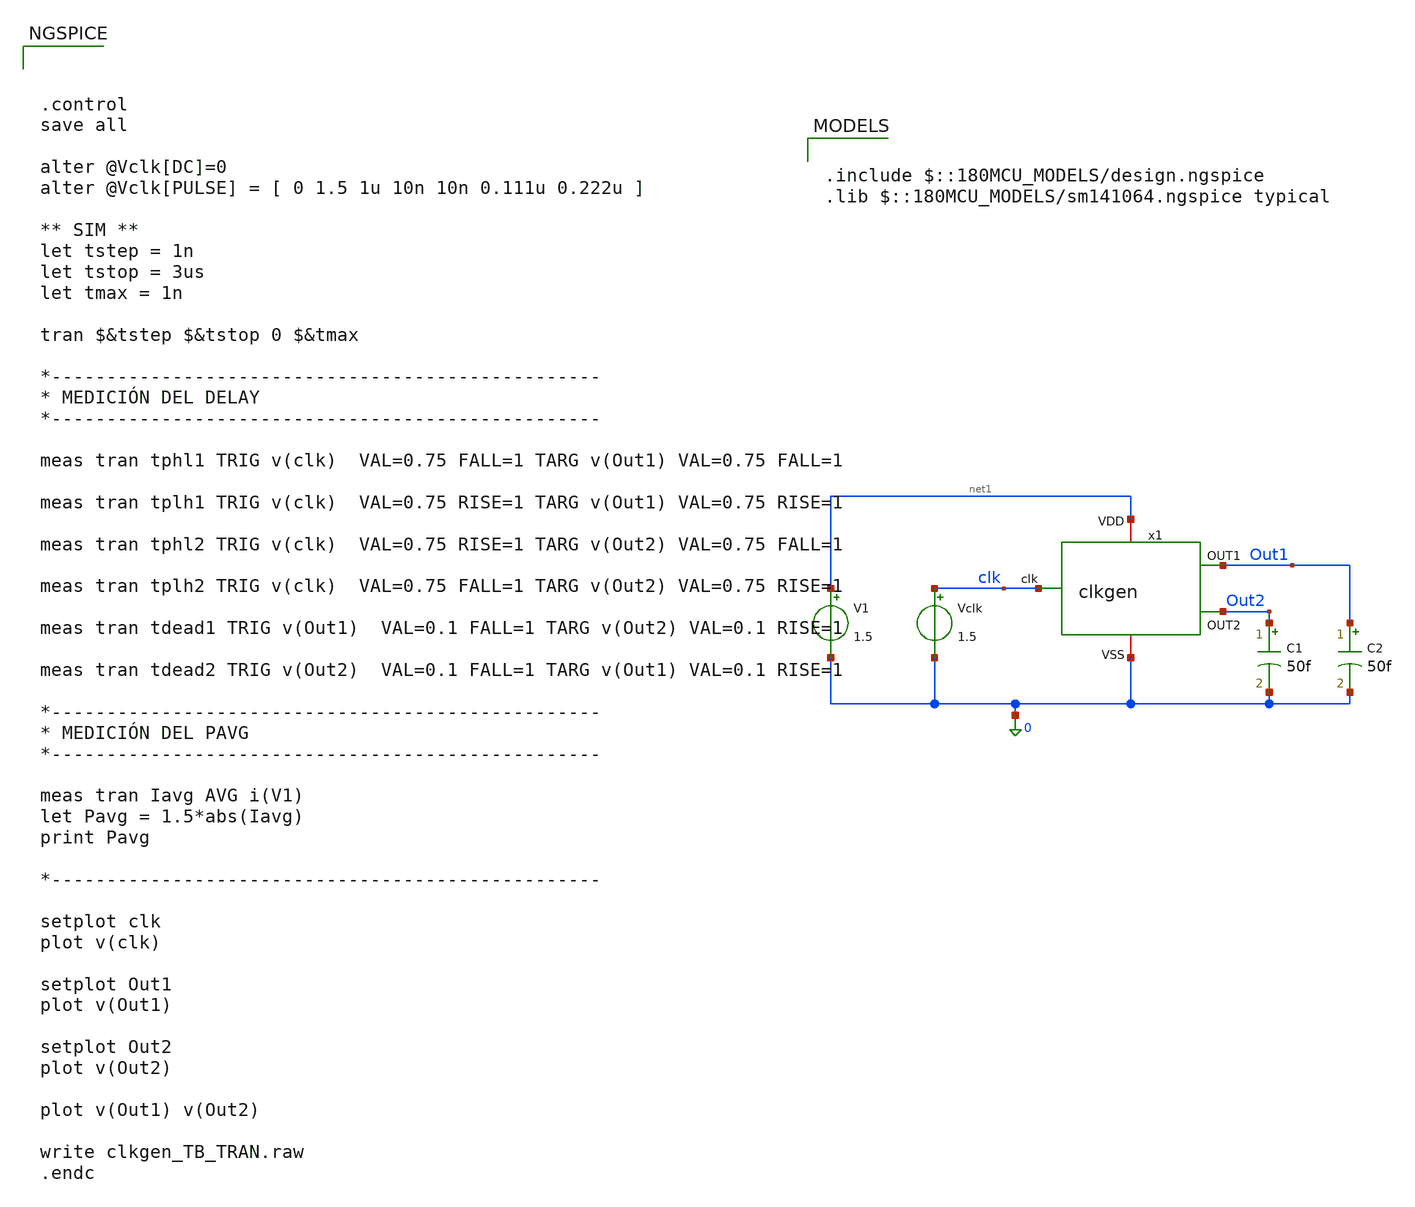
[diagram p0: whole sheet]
** sch_path: designs/DS_modulator/clkgen/xscheme/clkgen_TB_TRAN.sch
**.subckt clkgen_TB_TRAN
x1 net1 clk Out1 Out2 0 clkgen
V1 net1 0 1.5
Vclk clk 0 1.5
C1 Out2 0 50f m=1
C2 Out1 0 50f m=1
**** begin user architecture code

.include $::180MCU_MODELS/design.ngspice
.lib $::180MCU_MODELS/sm141064.ngspice typical




.control
save all

alter @Vclk[DC]=0
alter @Vclk[PULSE] = [ 0 1.5 1u 10n 10n 0.111u 0.222u ]

** SIM **
let tstep = 1n
let tstop = 3us
let tmax = 1n

tran $&tstep $&tstop 0 $&tmax

*--------------------------------------------------
* MEDICIÓN DEL DELAY
*--------------------------------------------------

meas tran tphl1 TRIG v(clk)  VAL=0.75 FALL=1 TARG v(Out1) VAL=0.75 FALL=1

meas tran tplh1 TRIG v(clk)  VAL=0.75 RISE=1 TARG v(Out1) VAL=0.75 RISE=1

meas tran tphl2 TRIG v(clk)  VAL=0.75 RISE=1 TARG v(Out2) VAL=0.75 FALL=1

meas tran tplh2 TRIG v(clk)  VAL=0.75 FALL=1 TARG v(Out2) VAL=0.75 RISE=1

meas tran tdead1 TRIG v(Out1)  VAL=0.1 FALL=1 TARG v(Out2) VAL=0.1 RISE=1

meas tran tdead2 TRIG v(Out2)  VAL=0.1 FALL=1 TARG v(Out1) VAL=0.1 RISE=1

*--------------------------------------------------
* MEDICIÓN DEL PAVG
*--------------------------------------------------

meas tran Iavg AVG i(V1)
let Pavg = 1.5*abs(Iavg)
print Pavg

*--------------------------------------------------

setplot clk
plot v(clk)

setplot Out1
plot v(Out1)

setplot Out2
plot v(Out2)

plot v(Out1) v(Out2)

write clkgen_TB_TRAN.raw
.endc


**** end user architecture code
**.ends

* expanding   symbol:
*+  chipaton/chipa2026_gf180mcu_DeltaSigma/designs/DS_modulator/clkgen/xscheme/clkgen.sym # of pins=5
** sym_path: chipaton/chipa2026_gf180mcu_DeltaSigma/designs/DS_modulator/clkgen/xscheme/clkgen.sym
** sch_path: chipaton/chipa2026_gf180mcu_DeltaSigma/designs/DS_modulator/clkgen/xscheme/clkgen.sch
.subckt clkgen VDD clk OUT1 OUT2 VSS
*.ipin clk
*.opin OUT1
*.opin OUT2
*.iopin VDD
*.iopin VSS
x1 VDD net3 net6 VSS gate_inv_L0d28
x2 VDD net4 net3 VSS gate_inv_L0d28
x3 VDD net1 net5 VSS gate_inv_L0d28
x4 VDD net2 net1 VSS gate_inv_L0d28
x5 VDD OUT2 net4 VSS gate_inv_L0d28
x6 VDD OUT1 net2 VSS gate_inv_L0d28
x7 VDD net7 clk VSS gate_inv_L0d28
x8 VDD net8 net9 net10 VDD clkgen_nand
x9 net11 net12 net13 net14 net15 clkgen_nand
.ends


* expanding   symbol:
*+  chipaton/chipa2026_gf180mcu_DeltaSigma/designs/DS_modulator/gate_inv_L0d28/xschem/gate_inv_L0d28.sym # of pins=4
** sym_path: chipaton/chipa2026_gf180mcu_DeltaSigma/designs/DS_modulator/gate_inv_L0d28/xschem/gate_inv_L0d28.sym
** sch_path: chipaton/chipa2026_gf180mcu_DeltaSigma/designs/DS_modulator/gate_inv_L0d28/xschem/gate_inv_L0d28.sch
.subckt gate_inv_L0d28 VDD B A VSS
*.opin B
*.ipin A
*.iopin VDD
*.iopin VSS
XMN B A VSS VSS nfet_03v3 L=0.28u W=1u nf=1 ad='int((nf+1)/2) * W/nf * 0.18u' as='int((nf+2)/2) * W/nf * 0.18u'
+ pd='2*int((nf+1)/2) * (W/nf + 0.18u)' ps='2*int((nf+2)/2) * (W/nf + 0.18u)' nrd='0.18u / W' nrs='0.18u / W'
+ sa=0 sb=0 sd=0 m=2
XMP B A VDD VDD pfet_03v3 L=0.28u W=3u nf=1 ad='int((nf+1)/2) * W/nf * 0.18u' as='int((nf+2)/2) * W/nf * 0.18u'
+ pd='2*int((nf+1)/2) * (W/nf + 0.18u)' ps='2*int((nf+2)/2) * (W/nf + 0.18u)' nrd='0.18u / W' nrs='0.18u / W'
+ sa=0 sb=0 sd=0 m=2
.ends


* expanding   symbol:
*+  chipaton/chipa2026_gf180mcu_DeltaSigma/designs/DS_modulator/clkgen/xscheme/clkgen_nand.sym # of pins=5
** sym_path: chipaton/chipa2026_gf180mcu_DeltaSigma/designs/DS_modulator/clkgen/xscheme/clkgen_nand.sym
** sch_path: chipaton/chipa2026_gf180mcu_DeltaSigma/designs/DS_modulator/clkgen/xscheme/clkgen_nand.sch
.subckt clkgen_nand VDD IN1 OUT IN2 VSS
*.ipin IN1
*.opin OUT
*.iopin VDD
*.ipin IN2
*.iopin VSS
XM1 net1 IN2 VSS VSS nfet_03v3 L=0.28u W=0.22u nf=1 ad='int((nf+1)/2) * W/nf * 0.18u' as='int((nf+2)/2) * W/nf * 0.18u'
+ pd='2*int((nf+1)/2) * (W/nf + 0.18u)' ps='2*int((nf+2)/2) * (W/nf + 0.18u)' nrd='0.18u / W' nrs='0.18u / W'
+ sa=0 sb=0 sd=0 m=1
XM2 OUT IN1 net1 VSS nfet_03v3 L=0.28u W=0.22u nf=1 ad='int((nf+1)/2) * W/nf * 0.18u' as='int((nf+2)/2) * W/nf * 0.18u'
+ pd='2*int((nf+1)/2) * (W/nf + 0.18u)' ps='2*int((nf+2)/2) * (W/nf + 0.18u)' nrd='0.18u / W' nrs='0.18u / W'
+ sa=0 sb=0 sd=0 m=1
XM3 OUT IN1 VDD VDD pfet_03v3 L=0.28u W=0.22u nf=1 ad='int((nf+1)/2) * W/nf * 0.18u' as='int((nf+2)/2) * W/nf * 0.18u'
+ pd='2*int((nf+1)/2) * (W/nf + 0.18u)' ps='2*int((nf+2)/2) * (W/nf + 0.18u)' nrd='0.18u / W' nrs='0.18u / W'
+ sa=0 sb=0 sd=0 m=1
XM5 OUT IN2 VDD VDD pfet_03v3 L=0.28u W=0.22u nf=1 ad='int((nf+1)/2) * W/nf * 0.18u' as='int((nf+2)/2) * W/nf * 0.18u'
+ pd='2*int((nf+1)/2) * (W/nf + 0.18u)' ps='2*int((nf+2)/2) * (W/nf + 0.18u)' nrd='0.18u / W' nrs='0.18u / W'
+ sa=0 sb=0 sd=0 m=1
.ends

.end
